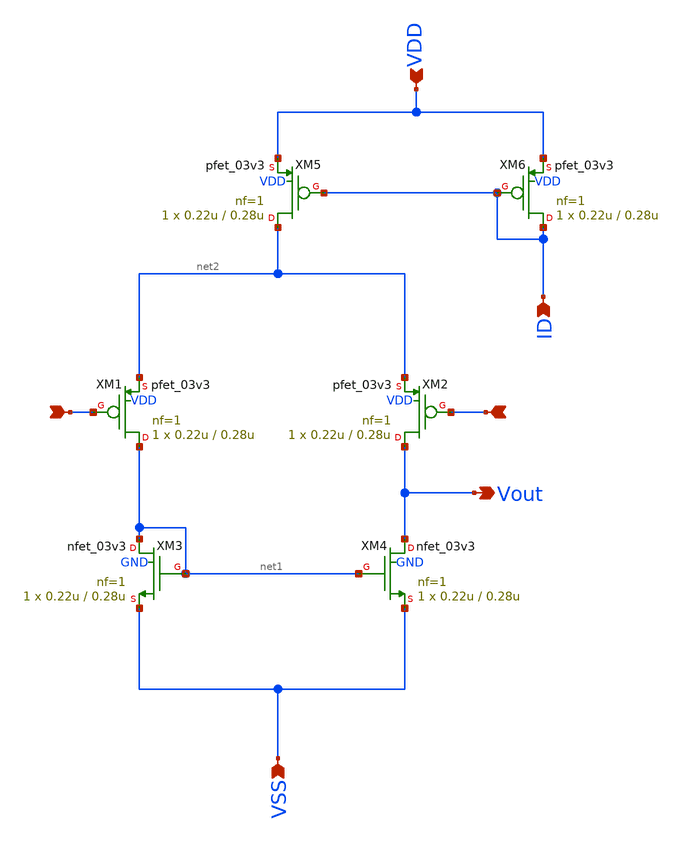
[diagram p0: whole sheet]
** sch_path: xschem/ota_miller/ota_p_in.sch
**.subckt ota_p_in Vout VSS VDD + - ID
*.opin Vout
*.ipin VSS
*.ipin VDD
*.ipin +
*.ipin -
*.ipin ID
XM1 net1 + net2 VDD pfet_03v3 L=0.28u W=0.22u nf=1 ad='int((nf+1)/2) * W/nf * 0.18u' as='int((nf+2)/2) * W/nf * 0.18u'
+ pd='2*int((nf+1)/2) * (W/nf + 0.18u)' ps='2*int((nf+2)/2) * (W/nf + 0.18u)' nrd='0.18u / W' nrs='0.18u / W'
+ sa=0 sb=0 sd=0 m=1 par=1
XM2 Vout - net2 VDD pfet_03v3 L=0.28u W=0.22u nf=1 ad='int((nf+1)/2) * W/nf * 0.18u' as='int((nf+2)/2) * W/nf * 0.18u'
+ pd='2*int((nf+1)/2) * (W/nf + 0.18u)' ps='2*int((nf+2)/2) * (W/nf + 0.18u)' nrd='0.18u / W' nrs='0.18u / W'
+ sa=0 sb=0 sd=0 m=1 par=1
XM3 net1 net1 VSS GND nfet_03v3 L=0.28u W=0.22u nf=1 ad='int((nf+1)/2) * W/nf * 0.18u' as='int((nf+2)/2) * W/nf * 0.18u'
+ pd='2*int((nf+1)/2) * (W/nf + 0.18u)' ps='2*int((nf+2)/2) * (W/nf + 0.18u)' nrd='0.18u / W' nrs='0.18u / W'
+ sa=0 sb=0 sd=0 m=1 par=1
XM4 Vout net1 VSS GND nfet_03v3 L=0.28u W=0.22u nf=1 ad='int((nf+1)/2) * W/nf * 0.18u' as='int((nf+2)/2) * W/nf * 0.18u'
+ pd='2*int((nf+1)/2) * (W/nf + 0.18u)' ps='2*int((nf+2)/2) * (W/nf + 0.18u)' nrd='0.18u / W' nrs='0.18u / W'
+ sa=0 sb=0 sd=0 m=1 par=1
XM5 net2 ID VDD VDD pfet_03v3 L=0.28u W=0.22u nf=1 ad='int((nf+1)/2) * W/nf * 0.18u' as='int((nf+2)/2) * W/nf * 0.18u'
+ pd='2*int((nf+1)/2) * (W/nf + 0.18u)' ps='2*int((nf+2)/2) * (W/nf + 0.18u)' nrd='0.18u / W' nrs='0.18u / W'
+ sa=0 sb=0 sd=0 m=1 par=1
XM6 ID ID VDD VDD pfet_03v3 L=0.28u W=0.22u nf=1 ad='int((nf+1)/2) * W/nf * 0.18u' as='int((nf+2)/2) * W/nf * 0.18u'
+ pd='2*int((nf+1)/2) * (W/nf + 0.18u)' ps='2*int((nf+2)/2) * (W/nf + 0.18u)' nrd='0.18u / W' nrs='0.18u / W'
+ sa=0 sb=0 sd=0 m=1 par=1
**.ends
.end
